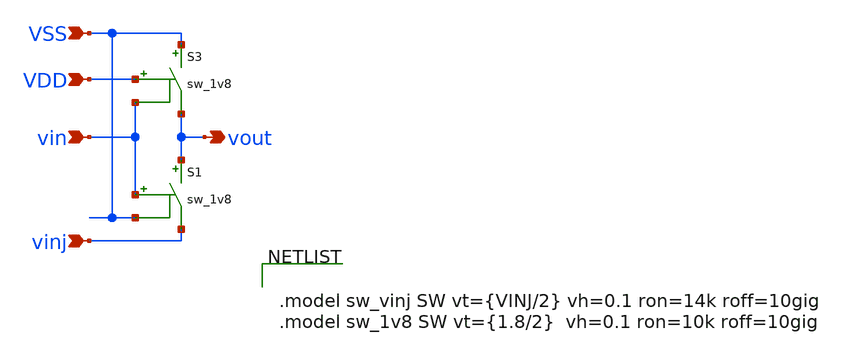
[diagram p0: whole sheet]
** sch_path: xschem/ideal_lsi1v8o6v0.sch
**.subckt ideal_lsi1v8o6v0 vin VDD VSS vinj vout
*.ipin vin
*.ipin VDD
*.ipin VSS
*.ipin vinj
*.opin vout
S1 vout vinj vin VSS sw_1v8
S3 VSS vout VDD vin sw_1v8
**** begin user architecture code


.model sw_vinj SW vt={VINJ/2} vh=0.1 ron=14k roff=10gig
.model sw_1v8 SW vt={1.8/2}  vh=0.1 ron=10k roff=10gig


**** end user architecture code
**.ends
.end
